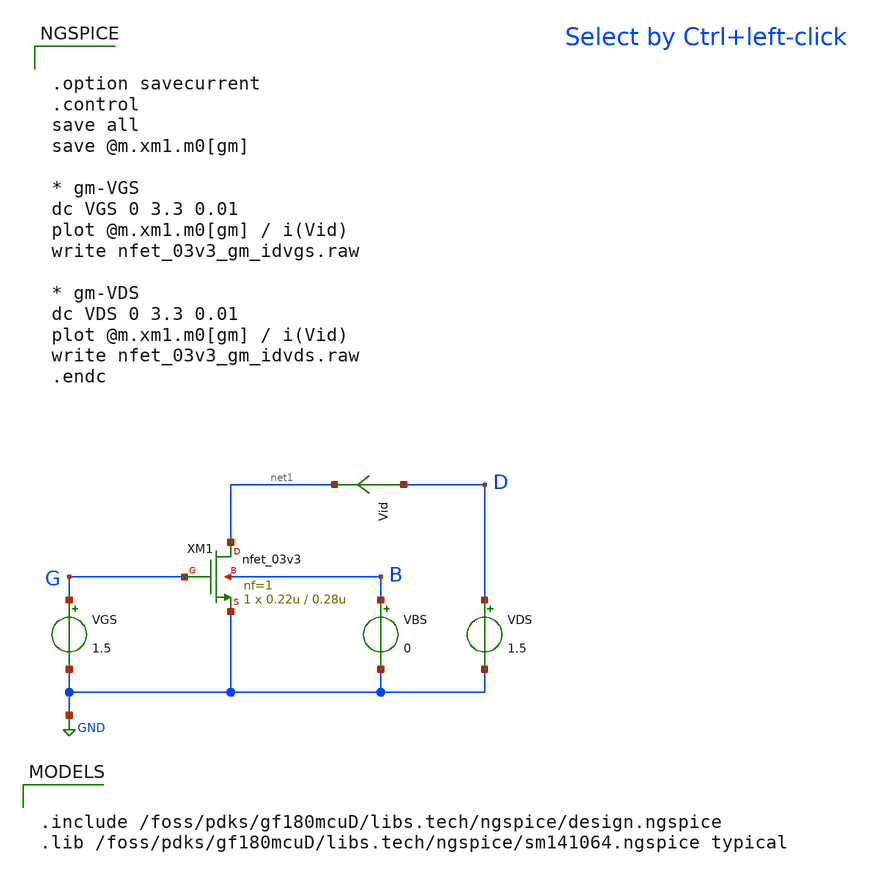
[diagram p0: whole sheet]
** sch_path: mosfet_gf180/nfet_03v3_gm.sch
**.subckt nfet_03v3_gm
XM1 net1 G GND B nfet_03v3 L=0.28u W=0.22u nf=1 ad='int((nf+1)/2) * W/nf * 0.18u' as='int((nf+2)/2) * W/nf * 0.18u'
+ pd='2*int((nf+1)/2) * (W/nf + 0.18u)' ps='2*int((nf+2)/2) * (W/nf + 0.18u)' nrd='0.18u / W' nrs='0.18u / W'
+ sa=0 sb=0 sd=0 m=1
VBS B GND 0
VGS G GND 1.5
VDS D GND 1.5
Vid D net1 0
.save i(vid)
**** begin user architecture code

.include /foss/pdks/gf180mcuD/libs.tech/ngspice/design.ngspice
.lib /foss/pdks/gf180mcuD/libs.tech/ngspice/sm141064.ngspice typical



.option savecurrent
.control
save all
save @m.xm1.m0[gm]

* gm-VGS
dc VGS 0 3.3 0.01
plot @m.xm1.m0[gm] / i(Vid)
write nfet_03v3_gm_idvgs.raw

* gm-VDS
dc VDS 0 3.3 0.01
plot @m.xm1.m0[gm] / i(Vid)
write nfet_03v3_gm_idvds.raw
.endc


**** end user architecture code
**.ends
.GLOBAL GND
.end
